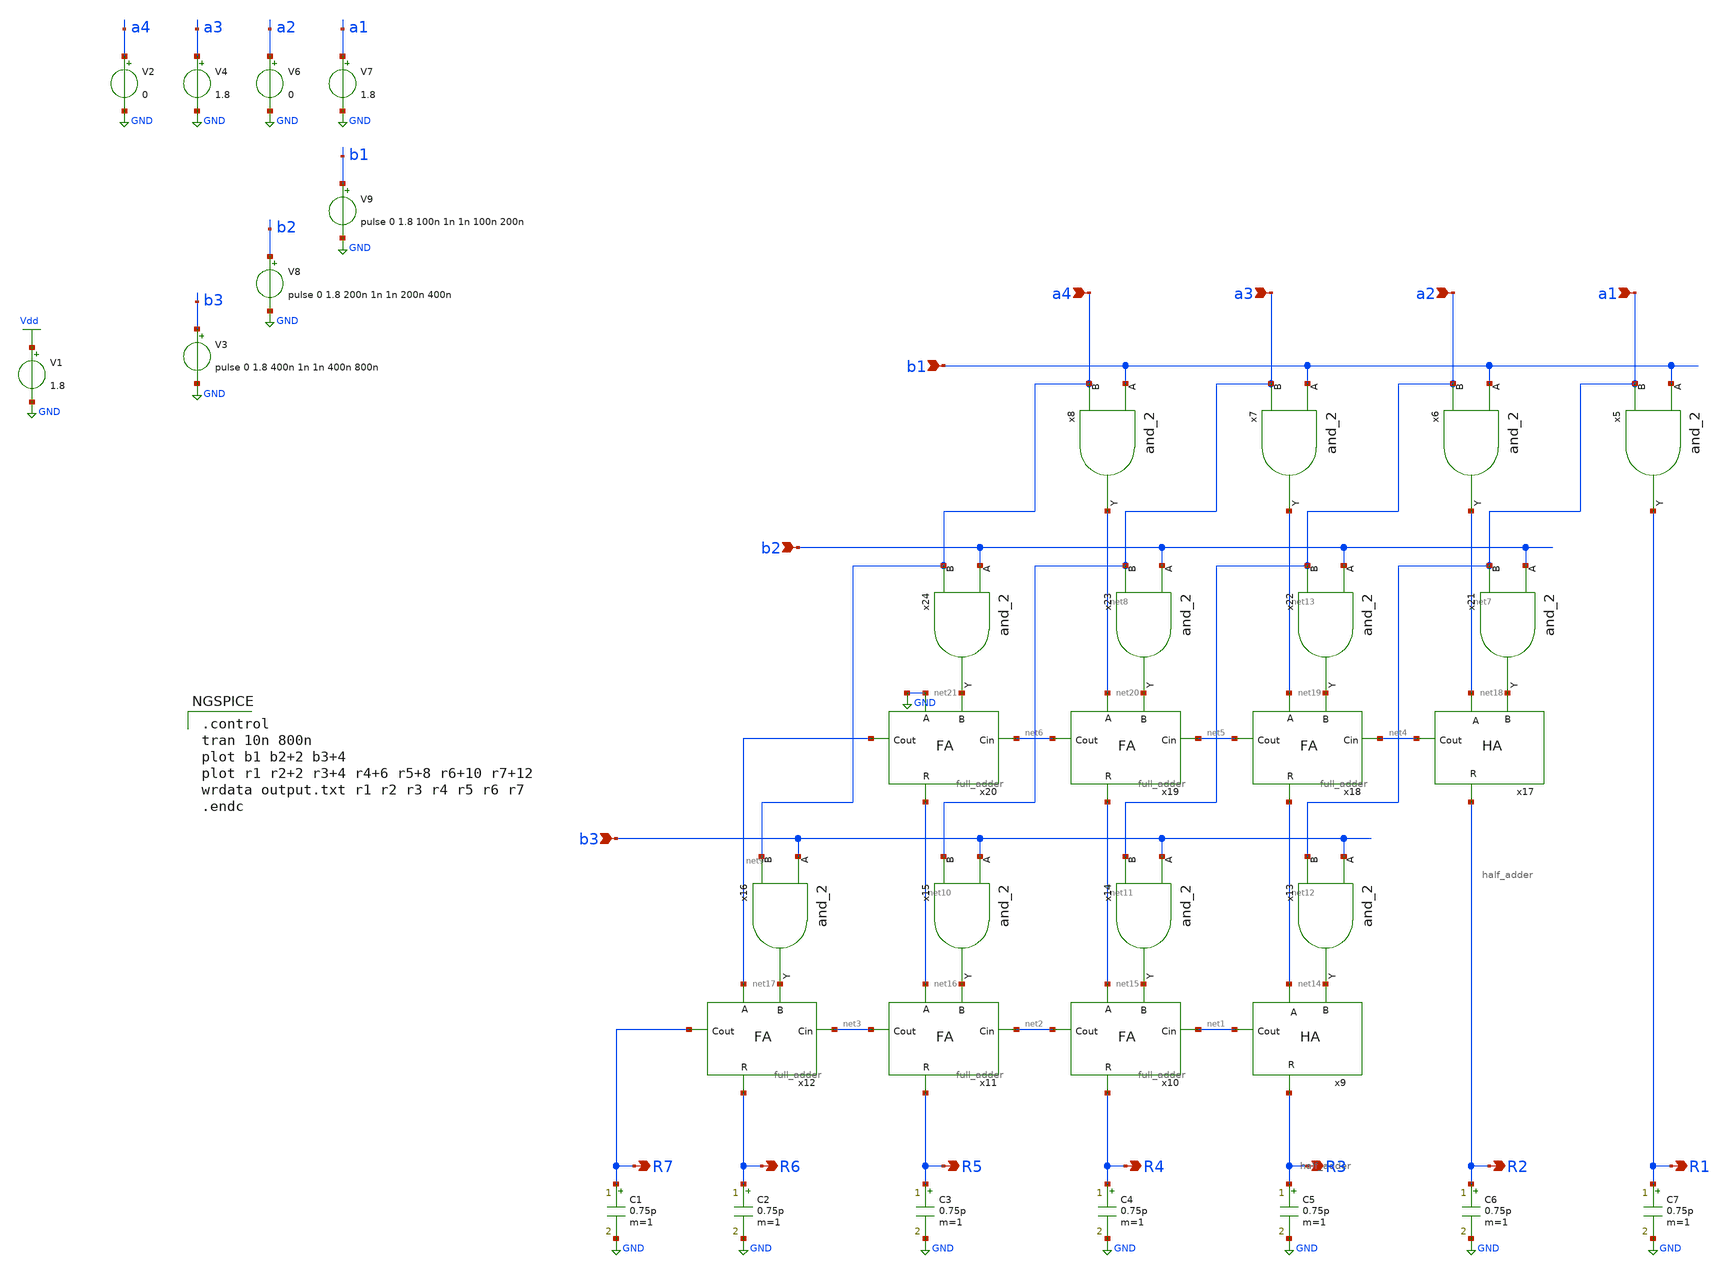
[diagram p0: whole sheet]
** sch_path: Circuiti/multiplier/test.sch
**.subckt test R7 R6 R5 R4 R3 R2 R1 a1 a2 a3 a4 b1 b2 b3
*.opin R7
*.opin R6
*.opin R5
*.opin R4
*.opin R3
*.opin R2
*.opin R1
*.ipin a1
*.ipin a2
*.ipin a3
*.ipin a4
*.ipin b1
*.ipin b2
*.ipin b3
V1 Vdd GND 1.8
x5 b1 R1 a1 and_2
x6 b1 net7 a2 and_2
x7 b1 net13 a3 and_2
x8 b1 net8 a4 and_2
x9 net12 R3 net14 net1 half_adder
x10 net11 net15 R4 net1 net2 full_adder
x11 net10 net16 R5 net2 net3 full_adder
x12 net9 net17 R6 net3 R7 full_adder
x13 b3 net14 a1 and_2
x14 b3 net15 a2 and_2
x15 b3 net16 a3 and_2
x16 b3 net17 a4 and_2
x17 net7 R2 net18 net4 half_adder
x18 net13 net19 net12 net4 net5 full_adder
x19 net8 net20 net11 net5 net6 full_adder
x20 GND net21 net10 net6 net9 full_adder
x21 b2 net18 a1 and_2
x22 b2 net19 a2 and_2
x23 b2 net20 a3 and_2
x24 b2 net21 a4 and_2
V2 a4 GND 0
V4 a3 GND 1.8
V6 a2 GND 0
V7 a1 GND 1.8
V8 b2 GND pulse 0 1.8 200n 1n 1n 200n 400n
V9 b1 GND pulse 0 1.8 100n 1n 1n 100n 200n
V3 b3 GND pulse 0 1.8 400n 1n 1n 400n 800n
C1 R7 GND 0.75p m=1
C2 R6 GND 0.75p m=1
C3 R5 GND 0.75p m=1
C4 R4 GND 0.75p m=1
C5 R3 GND 0.75p m=1
C6 R2 GND 0.75p m=1
C7 R1 GND 0.75p m=1
**** begin user architecture code


.lib /home/matteo/xschem_downloads/skywater-pdk/libraries/sky130_fd_pr_ngspice/latest/models/sky130.lib.spice tt

*.include /home/matteo/xschem_downloads/skywater-pdk/libraries/sky130_fd_pr_ngspice/latest/cells/nfet_01v8/sky130_fd_pr__nfet_01v8__tt.corner.spice

.param mc_mm_switch=0
.param mc_pr_switch=1



.control
tran 10n 800n
plot b1 b2+2 b3+4
plot r1 r2+2 r3+4 r4+6 r5+8 r6+10 r7+12
wrdata output.txt r1 r2 r3 r4 r5 r6 r7
.endc



.ic v(r1)=0
.ic v(r2)=0
.ic v(r3)=0
.ic v(r4)=0

**** end user architecture code
**.ends

* expanding   symbol:  /home/matteo/Documenti/tesi/Circuiti/logic_gates_sch_sym/and_2.sym # of
*+ pins=3
** sym_path: Circuiti/logic_gates_sch_sym/and_2.sym
** sch_path: Circuiti/logic_gates_sch_sym/and_2.sch
.subckt and_2 A Y B
*.ipin B
*.ipin A
*.opin Y
x1 A net1 B nand_2
x2 net1 Y not
.ends


* expanding   symbol:  /home/matteo/Documenti/tesi/Circuiti/multiplier/half_adder.sym # of pins=4
** sym_path: Circuiti/multiplier/half_adder.sym
** sch_path: Circuiti/multiplier/half_adder.sch
.subckt half_adder A R B Cout
*.ipin A
*.ipin B
*.opin R
*.opin Cout
x1 A R B xor_2
x2 A Cout B and_2
.ends


* expanding   symbol:  /home/matteo/Documenti/tesi/Circuiti/multiplier/full_adder.sym # of pins=5
** sym_path: Circuiti/multiplier/full_adder.sym
** sch_path: Circuiti/multiplier/full_adder.sch
.subckt full_adder A B R Cin Cout
*.ipin A
*.ipin B
*.ipin Cin
*.opin R
*.opin Cout
x1 A net1 B xor_2
x2 net1 net2 Cin and_2
x3 net2 Cout net3 or_2
x4 net1 R Cin xor_2
x5 A net3 B and_2
.ends


* expanding   symbol:  /home/matteo/Documenti/tesi/Circuiti/logic_gates_sch_sym/nand_2.sym # of
*+ pins=3
** sym_path: Circuiti/logic_gates_sch_sym/nand_2.sym
** sch_path: Circuiti/logic_gates_sch_sym/nand_2.sch
.subckt nand_2 A Y B
*.ipin A
*.ipin B
*.opin Y
XM1 Y A net1 GND sky130_fd_pr__nfet_01v8 L=0.15 W=1 nf=1 ad='int((nf+1)/2) * W/nf * 0.29' as='int((nf+2)/2) * W/nf * 0.29'
+ pd='2*int((nf+1)/2) * (W/nf + 0.29)' ps='2*int((nf+2)/2) * (W/nf + 0.29)' nrd='0.29 / W' nrs='0.29 / W'
+ sa=0 sb=0 sd=0 mult=1 m=1
XM3 Y B Vdd VDD sky130_fd_pr__pfet_01v8 L=0.45 W=4.8 nf=1 ad='int((nf+1)/2) * W/nf * 0.29' as='int((nf+2)/2) * W/nf * 0.29'
+ pd='2*int((nf+1)/2) * (W/nf + 0.29)' ps='2*int((nf+2)/2) * (W/nf + 0.29)' nrd='0.29 / W' nrs='0.29 / W'
+ sa=0 sb=0 sd=0 mult=1 m=1
XM4 Y A Vdd VDD sky130_fd_pr__pfet_01v8 L=0.45 W=4.8 nf=1 ad='int((nf+1)/2) * W/nf * 0.29' as='int((nf+2)/2) * W/nf * 0.29'
+ pd='2*int((nf+1)/2) * (W/nf + 0.29)' ps='2*int((nf+2)/2) * (W/nf + 0.29)' nrd='0.29 / W' nrs='0.29 / W'
+ sa=0 sb=0 sd=0 mult=1 m=1
XM2 net1 B GND GND sky130_fd_pr__nfet_01v8 L=0.15 W=1 nf=1 ad='int((nf+1)/2) * W/nf * 0.29' as='int((nf+2)/2) * W/nf * 0.29'
+ pd='2*int((nf+1)/2) * (W/nf + 0.29)' ps='2*int((nf+2)/2) * (W/nf + 0.29)' nrd='0.29 / W' nrs='0.29 / W'
+ sa=0 sb=0 sd=0 mult=1 m=1
.ends


* expanding   symbol:  /home/matteo/Documenti/tesi/Circuiti/logic_gates_sch_sym/not.sym # of pins=2
** sym_path: Circuiti/logic_gates_sch_sym/not.sym
** sch_path: Circuiti/logic_gates_sch_sym/not.sch
.subckt not A Y
*.ipin A
*.opin Y
XM1 Y A GND GND sky130_fd_pr__nfet_01v8 L=0.45 W=1 nf=1 ad='int((nf+1)/2) * W/nf * 0.29' as='int((nf+2)/2) * W/nf * 0.29'
+ pd='2*int((nf+1)/2) * (W/nf + 0.29)' ps='2*int((nf+2)/2) * (W/nf + 0.29)' nrd='0.29 / W' nrs='0.29 / W'
+ sa=0 sb=0 sd=0 mult=1 m=1
XM2 Y A Vdd VDD sky130_fd_pr__pfet_01v8 L=0.45 W=4.8 nf=1 ad='int((nf+1)/2) * W/nf * 0.29' as='int((nf+2)/2) * W/nf * 0.29'
+ pd='2*int((nf+1)/2) * (W/nf + 0.29)' ps='2*int((nf+2)/2) * (W/nf + 0.29)' nrd='0.29 / W' nrs='0.29 / W'
+ sa=0 sb=0 sd=0 mult=1 m=1
.ends


* expanding   symbol:  /home/matteo/Documenti/tesi/Circuiti/logic_gates_sch_sym/xor_2.sym # of
*+ pins=3
** sym_path: Circuiti/logic_gates_sch_sym/xor_2.sym
** sch_path: Circuiti/logic_gates_sch_sym/xor_2.sch
.subckt xor_2 A Y B
*.ipin A
*.ipin B
*.opin Y
x1 A net1 B nand_2
x2 A net2 B or_2
x3 net1 Y net2 and_2
.ends


* expanding   symbol:  /home/matteo/Documenti/tesi/Circuiti/logic_gates_sch_sym/or_2.sym # of pins=3
** sym_path: Circuiti/logic_gates_sch_sym/or_2.sym
** sch_path: Circuiti/logic_gates_sch_sym/or_2.sch
.subckt or_2 A Y B
*.ipin A
*.ipin B
*.opin Y
x1 A net1 B nor_2
x2 net1 Y not
.ends


* expanding   symbol:  /home/matteo/Documenti/tesi/Circuiti/logic_gates_sch_sym/nor_2.sym # of
*+ pins=3
** sym_path: Circuiti/logic_gates_sch_sym/nor_2.sym
** sch_path: Circuiti/logic_gates_sch_sym/nor_2.sch
.subckt nor_2 A Y B
*.opin Y
*.ipin A
*.ipin B
XM1 Y B GND GND sky130_fd_pr__nfet_01v8 L=0.45 W=1 nf=1 ad='int((nf+1)/2) * W/nf * 0.29' as='int((nf+2)/2) * W/nf * 0.29'
+ pd='2*int((nf+1)/2) * (W/nf + 0.29)' ps='2*int((nf+2)/2) * (W/nf + 0.29)' nrd='0.29 / W' nrs='0.29 / W'
+ sa=0 sb=0 sd=0 mult=1 m=1
XM3 Y B net1 VDD sky130_fd_pr__pfet_01v8 L=0.15 W=4.8 nf=1 ad='int((nf+1)/2) * W/nf * 0.29' as='int((nf+2)/2) * W/nf * 0.29'
+ pd='2*int((nf+1)/2) * (W/nf + 0.29)' ps='2*int((nf+2)/2) * (W/nf + 0.29)' nrd='0.29 / W' nrs='0.29 / W'
+ sa=0 sb=0 sd=0 mult=1 m=1
XM4 net1 A Vdd VDD sky130_fd_pr__pfet_01v8 L=0.15 W=4.8 nf=1 ad='int((nf+1)/2) * W/nf * 0.29' as='int((nf+2)/2) * W/nf * 0.29'
+ pd='2*int((nf+1)/2) * (W/nf + 0.29)' ps='2*int((nf+2)/2) * (W/nf + 0.29)' nrd='0.29 / W' nrs='0.29 / W'
+ sa=0 sb=0 sd=0 mult=1 m=1
XM2 Y A GND GND sky130_fd_pr__nfet_01v8 L=0.45 W=1 nf=1 ad='int((nf+1)/2) * W/nf * 0.29' as='int((nf+2)/2) * W/nf * 0.29'
+ pd='2*int((nf+1)/2) * (W/nf + 0.29)' ps='2*int((nf+2)/2) * (W/nf + 0.29)' nrd='0.29 / W' nrs='0.29 / W'
+ sa=0 sb=0 sd=0 mult=1 m=1
.ends

.GLOBAL GND
.GLOBAL Vdd
.end
